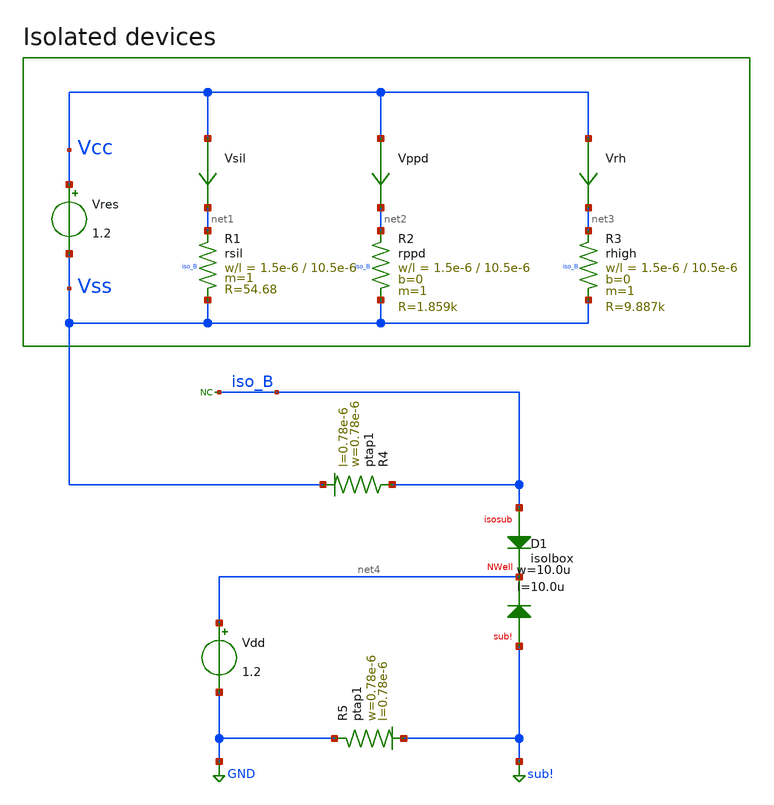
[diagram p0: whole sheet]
** sch_path: ihp-sg13g2/xschem_libs/sg13g2_tests_ase/iso_dc_res/schematic/iso_dc_res.sch
* Copyright 2023 IHP PDK Authors
**.subckt iso_dc_res
Vres Vcc Vss 1.2
Vsil Vcc net1 0
.save i(vsil)
Vppd Vcc net2 0
.save i(vppd)
Vrh Vcc net3 0
.save i(vrh)
XR1 net1 Vss iso_B rsil w=1.5e-6 l=10.5e-6 m=1 mm_ok=1
XR2 net2 Vss iso_B rppd w=1.5e-6 l=10.5e-6 m=1 b=0 mm_ok=1
XR3 net3 Vss iso_B rhigh w=1.5e-6 l=10.5e-6 m=1 b=0 mm_ok=1
XR5 GND sub! ptap1 R=262.8 w=0.78e-6 l=0.78e-6
Vdd net4 GND 1.2
XD1 iso_B net4 sub! isolbox l=10.0u w=10.0u
* noconn iso_B
XR4 iso_B Vss ptap1 R=262.8 w=0.78e-6 l=0.78e-6
**.ends
.GLOBAL GND
.GLOBAL sub!
.end
